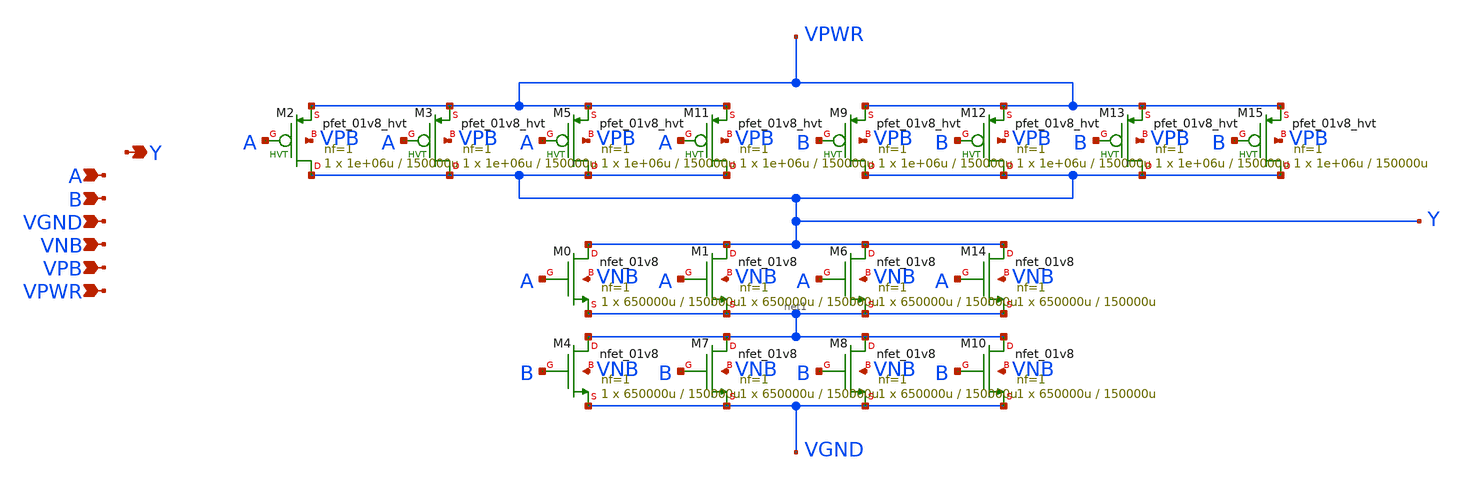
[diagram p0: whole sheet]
** sch_path: schematics/nand2/sky130_fd_sc_hd__nand2_4.sch
**.subckt sky130_fd_sc_hd__nand2_4 A B VGND VNB VPB VPWR Y
*.ipin A
*.ipin B
*.ipin VGND
*.ipin VNB
*.ipin VPB
*.ipin VPWR
*.opin Y
XM2 Y A VPWR VPB sky130_fd_pr__pfet_01v8_hvt L=150000u W=1e+06u nf=1 ad='int((1 + 1)/2) * 1e+06u / 1 * 0.29'
+ as='int((1 + 2)/2) * 1e+06u / 1 * 0.29' pd='2*int((1 + 1)/2) * (1e+06u / 1 + 0.29)' ps='2*int((1 + 2)/2) * (1e+06u / 1 + 0.29)'
+ nrd='0.29 / 1e+06u ' nrs='0.29 / 1e+06u ' sa=0 sb=0 sd=0 mult=1 m=1
XM3 Y A VPWR VPB sky130_fd_pr__pfet_01v8_hvt L=150000u W=1e+06u nf=1 ad='int((1 + 1)/2) * 1e+06u / 1 * 0.29'
+ as='int((1 + 2)/2) * 1e+06u / 1 * 0.29' pd='2*int((1 + 1)/2) * (1e+06u / 1 + 0.29)' ps='2*int((1 + 2)/2) * (1e+06u / 1 + 0.29)'
+ nrd='0.29 / 1e+06u ' nrs='0.29 / 1e+06u ' sa=0 sb=0 sd=0 mult=1 m=1
XM5 Y A VPWR VPB sky130_fd_pr__pfet_01v8_hvt L=150000u W=1e+06u nf=1 ad='int((1 + 1)/2) * 1e+06u / 1 * 0.29'
+ as='int((1 + 2)/2) * 1e+06u / 1 * 0.29' pd='2*int((1 + 1)/2) * (1e+06u / 1 + 0.29)' ps='2*int((1 + 2)/2) * (1e+06u / 1 + 0.29)'
+ nrd='0.29 / 1e+06u ' nrs='0.29 / 1e+06u ' sa=0 sb=0 sd=0 mult=1 m=1
XM11 Y A VPWR VPB sky130_fd_pr__pfet_01v8_hvt L=150000u W=1e+06u nf=1 ad='int((1 + 1)/2) * 1e+06u / 1 * 0.29'
+ as='int((1 + 2)/2) * 1e+06u / 1 * 0.29' pd='2*int((1 + 1)/2) * (1e+06u / 1 + 0.29)' ps='2*int((1 + 2)/2) * (1e+06u / 1 + 0.29)'
+ nrd='0.29 / 1e+06u ' nrs='0.29 / 1e+06u ' sa=0 sb=0 sd=0 mult=1 m=1
XM9 Y B VPWR VPB sky130_fd_pr__pfet_01v8_hvt L=150000u W=1e+06u nf=1 ad='int((1 + 1)/2) * 1e+06u / 1 * 0.29'
+ as='int((1 + 2)/2) * 1e+06u / 1 * 0.29' pd='2*int((1 + 1)/2) * (1e+06u / 1 + 0.29)' ps='2*int((1 + 2)/2) * (1e+06u / 1 + 0.29)'
+ nrd='0.29 / 1e+06u ' nrs='0.29 / 1e+06u ' sa=0 sb=0 sd=0 mult=1 m=1
XM12 Y B VPWR VPB sky130_fd_pr__pfet_01v8_hvt L=150000u W=1e+06u nf=1 ad='int((1 + 1)/2) * 1e+06u / 1 * 0.29'
+ as='int((1 + 2)/2) * 1e+06u / 1 * 0.29' pd='2*int((1 + 1)/2) * (1e+06u / 1 + 0.29)' ps='2*int((1 + 2)/2) * (1e+06u / 1 + 0.29)'
+ nrd='0.29 / 1e+06u ' nrs='0.29 / 1e+06u ' sa=0 sb=0 sd=0 mult=1 m=1
XM13 Y B VPWR VPB sky130_fd_pr__pfet_01v8_hvt L=150000u W=1e+06u nf=1 ad='int((1 + 1)/2) * 1e+06u / 1 * 0.29'
+ as='int((1 + 2)/2) * 1e+06u / 1 * 0.29' pd='2*int((1 + 1)/2) * (1e+06u / 1 + 0.29)' ps='2*int((1 + 2)/2) * (1e+06u / 1 + 0.29)'
+ nrd='0.29 / 1e+06u ' nrs='0.29 / 1e+06u ' sa=0 sb=0 sd=0 mult=1 m=1
XM15 Y B VPWR VPB sky130_fd_pr__pfet_01v8_hvt L=150000u W=1e+06u nf=1 ad='int((1 + 1)/2) * 1e+06u / 1 * 0.29'
+ as='int((1 + 2)/2) * 1e+06u / 1 * 0.29' pd='2*int((1 + 1)/2) * (1e+06u / 1 + 0.29)' ps='2*int((1 + 2)/2) * (1e+06u / 1 + 0.29)'
+ nrd='0.29 / 1e+06u ' nrs='0.29 / 1e+06u ' sa=0 sb=0 sd=0 mult=1 m=1
XM0 Y A net1 VNB sky130_fd_pr__nfet_01v8 L=150000u W=650000u nf=1 ad='int((1 + 1)/2) * 650000u / 1 * 0.29'
+ as='int((1 + 2)/2) * 650000u / 1 * 0.29' pd='2*int((1 + 1)/2) * (650000u / 1 + 0.29)' ps='2*int((1 + 2)/2) * (650000u / 1 + 0.29)'
+ nrd='0.29 / 650000u ' nrs='0.29 / 650000u ' sa=0 sb=0 sd=0 mult=1 m=1
XM1 Y A net1 VNB sky130_fd_pr__nfet_01v8 L=150000u W=650000u nf=1 ad='int((1 + 1)/2) * 650000u / 1 * 0.29'
+ as='int((1 + 2)/2) * 650000u / 1 * 0.29' pd='2*int((1 + 1)/2) * (650000u / 1 + 0.29)' ps='2*int((1 + 2)/2) * (650000u / 1 + 0.29)'
+ nrd='0.29 / 650000u ' nrs='0.29 / 650000u ' sa=0 sb=0 sd=0 mult=1 m=1
XM6 Y A net1 VNB sky130_fd_pr__nfet_01v8 L=150000u W=650000u nf=1 ad='int((1 + 1)/2) * 650000u / 1 * 0.29'
+ as='int((1 + 2)/2) * 650000u / 1 * 0.29' pd='2*int((1 + 1)/2) * (650000u / 1 + 0.29)' ps='2*int((1 + 2)/2) * (650000u / 1 + 0.29)'
+ nrd='0.29 / 650000u ' nrs='0.29 / 650000u ' sa=0 sb=0 sd=0 mult=1 m=1
XM14 Y A net1 VNB sky130_fd_pr__nfet_01v8 L=150000u W=650000u nf=1 ad='int((1 + 1)/2) * 650000u / 1 * 0.29'
+ as='int((1 + 2)/2) * 650000u / 1 * 0.29' pd='2*int((1 + 1)/2) * (650000u / 1 + 0.29)' ps='2*int((1 + 2)/2) * (650000u / 1 + 0.29)'
+ nrd='0.29 / 650000u ' nrs='0.29 / 650000u ' sa=0 sb=0 sd=0 mult=1 m=1
XM4 net1 B VGND VNB sky130_fd_pr__nfet_01v8 L=150000u W=650000u nf=1 ad='int((1 + 1)/2) * 650000u / 1 * 0.29'
+ as='int((1 + 2)/2) * 650000u / 1 * 0.29' pd='2*int((1 + 1)/2) * (650000u / 1 + 0.29)' ps='2*int((1 + 2)/2) * (650000u / 1 + 0.29)'
+ nrd='0.29 / 650000u ' nrs='0.29 / 650000u ' sa=0 sb=0 sd=0 mult=1 m=1
XM7 net1 B VGND VNB sky130_fd_pr__nfet_01v8 L=150000u W=650000u nf=1 ad='int((1 + 1)/2) * 650000u / 1 * 0.29'
+ as='int((1 + 2)/2) * 650000u / 1 * 0.29' pd='2*int((1 + 1)/2) * (650000u / 1 + 0.29)' ps='2*int((1 + 2)/2) * (650000u / 1 + 0.29)'
+ nrd='0.29 / 650000u ' nrs='0.29 / 650000u ' sa=0 sb=0 sd=0 mult=1 m=1
XM8 net1 B VGND VNB sky130_fd_pr__nfet_01v8 L=150000u W=650000u nf=1 ad='int((1 + 1)/2) * 650000u / 1 * 0.29'
+ as='int((1 + 2)/2) * 650000u / 1 * 0.29' pd='2*int((1 + 1)/2) * (650000u / 1 + 0.29)' ps='2*int((1 + 2)/2) * (650000u / 1 + 0.29)'
+ nrd='0.29 / 650000u ' nrs='0.29 / 650000u ' sa=0 sb=0 sd=0 mult=1 m=1
XM10 net1 B VGND VNB sky130_fd_pr__nfet_01v8 L=150000u W=650000u nf=1 ad='int((1 + 1)/2) * 650000u / 1 * 0.29'
+ as='int((1 + 2)/2) * 650000u / 1 * 0.29' pd='2*int((1 + 1)/2) * (650000u / 1 + 0.29)' ps='2*int((1 + 2)/2) * (650000u / 1 + 0.29)'
+ nrd='0.29 / 650000u ' nrs='0.29 / 650000u ' sa=0 sb=0 sd=0 mult=1 m=1
**.ends
.end
